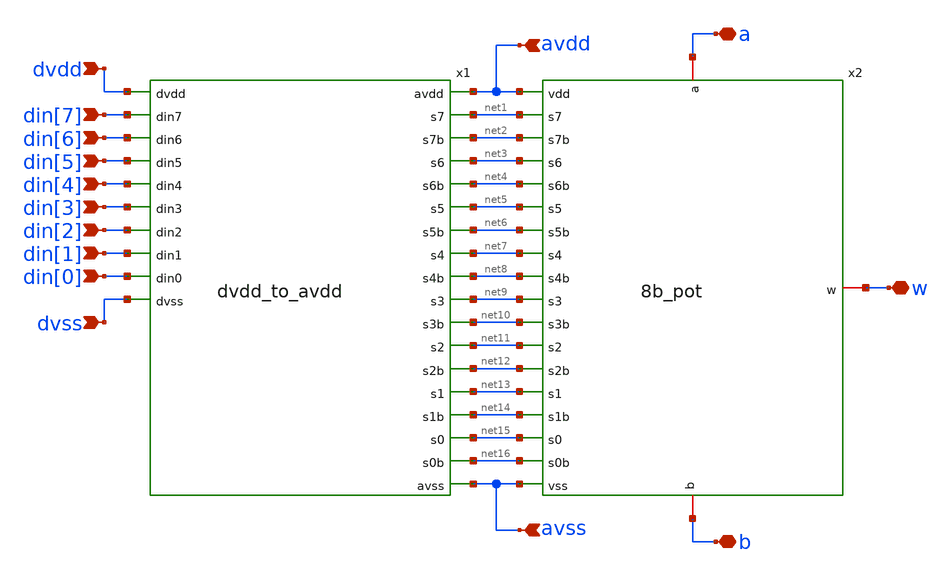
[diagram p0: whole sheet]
** sch_path: xschem/sky130_di_ip__rheostat_8bit.sch
**.subckt sky130_di_ip__rheostat_8bit avdd dvdd dvss avss b w a din[0] din[1] din[2] din[3] din[4]
*+ din[5] din[6] din[7]
*.ipin avdd
*.ipin dvdd
*.ipin dvss
*.ipin avss
*.iopin b
*.iopin w
*.iopin a
*.ipin din[0]
*.ipin din[1]
*.ipin din[2]
*.ipin din[3]
*.ipin din[4]
*.ipin din[5]
*.ipin din[6]
*.ipin din[7]
x1 avdd dvdd net1 din[7] net2 net3 din[6] net4 net5 din[5] net6 net7 din[4] net8 net9 din[3] net10
+ net11 din[2] net12 net13 din[1] net14 net15 din[0] net16 dvss avss dvdd_to_avdd
x2 avdd a net1 net2 net3 net4 net5 net6 net7 net8 w net9 net10 net11 net12 net13 net14 net15 net16 b
+ avss 8b_pot
**.ends
.end
